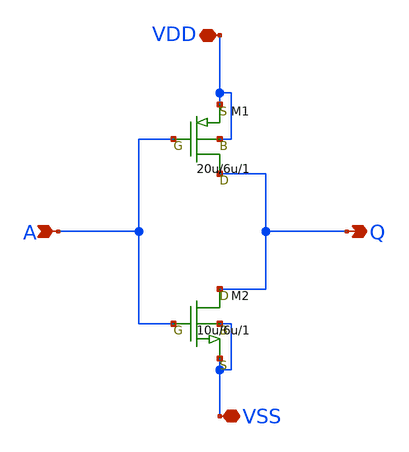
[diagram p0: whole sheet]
** sch_path: samples/inverter/MF20/inverter.sch
**.subckt inverter VDD VSS A Q
*.iopin VDD
*.iopin VSS
*.ipin A
*.opin Q
M1 Q A VDD VDD pch w=20u l=6u as=0 ps=0 ad=0 pd=0 m=1
M2 Q A VSS VSS nch w=10u l=6u as=0 ps=0 ad=0 pd=0 m=1
**.ends
.end
